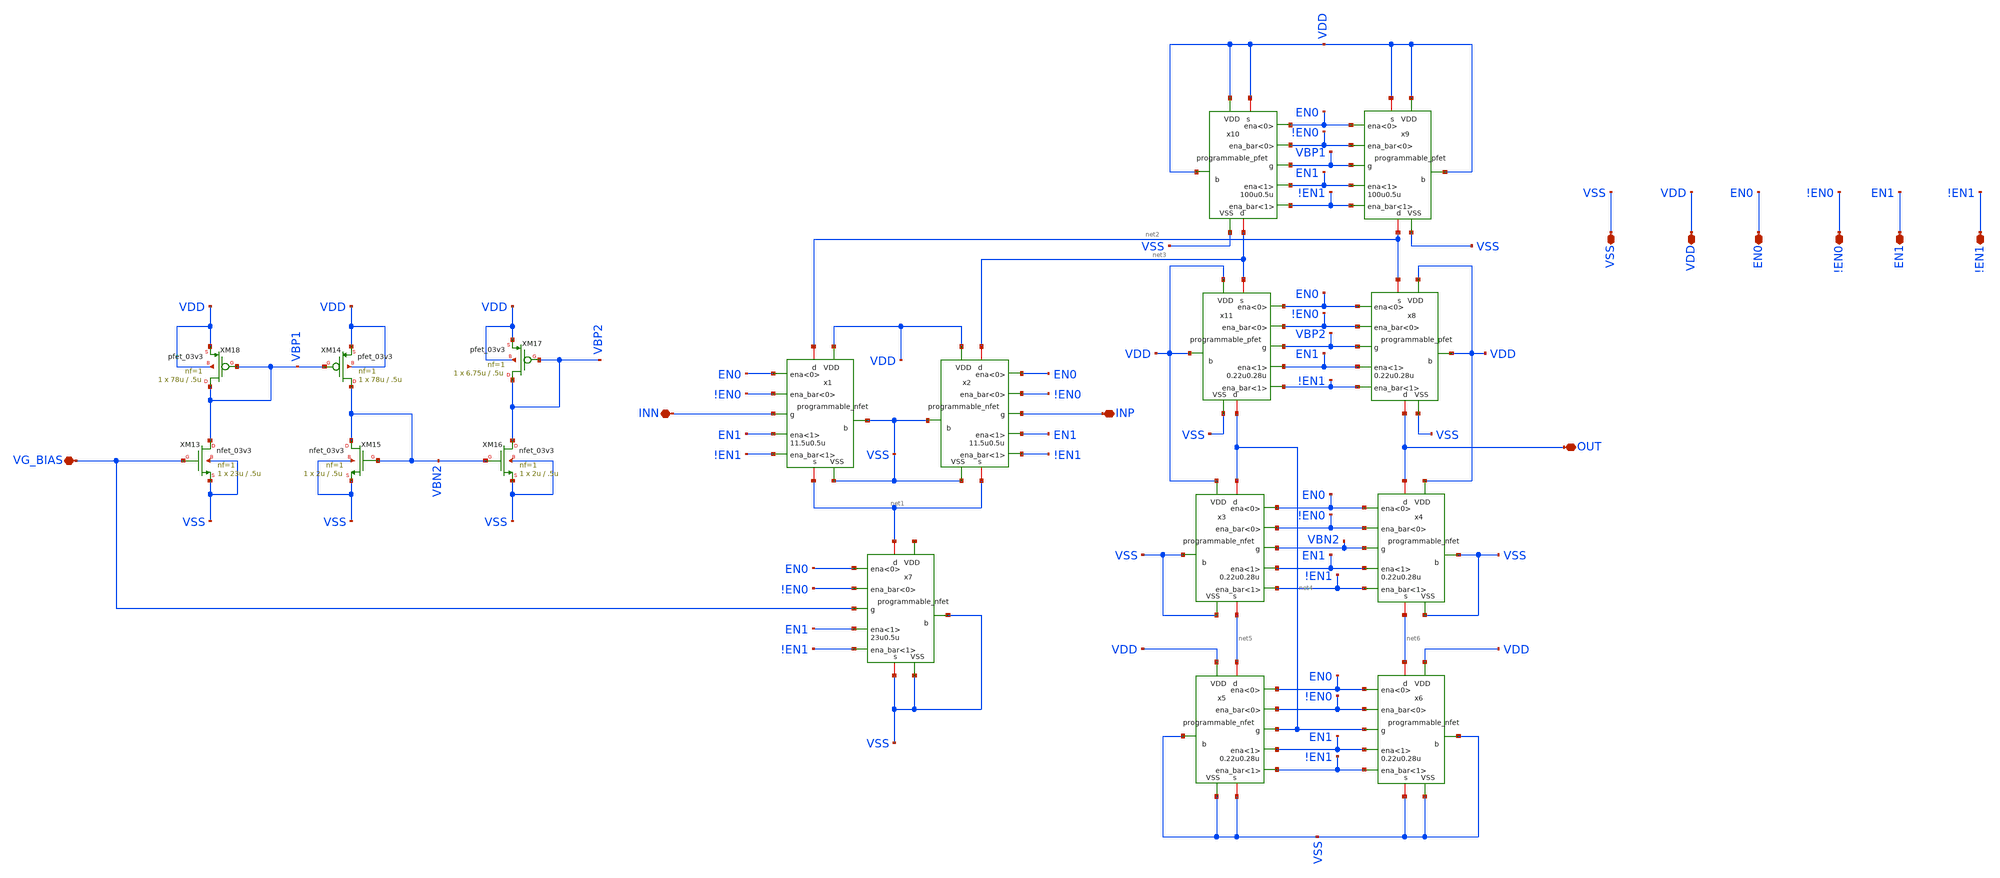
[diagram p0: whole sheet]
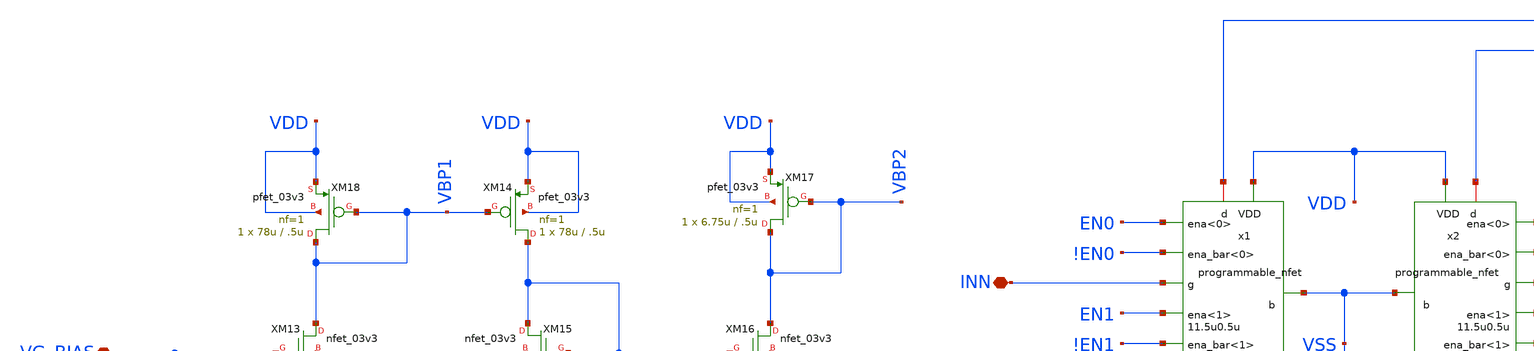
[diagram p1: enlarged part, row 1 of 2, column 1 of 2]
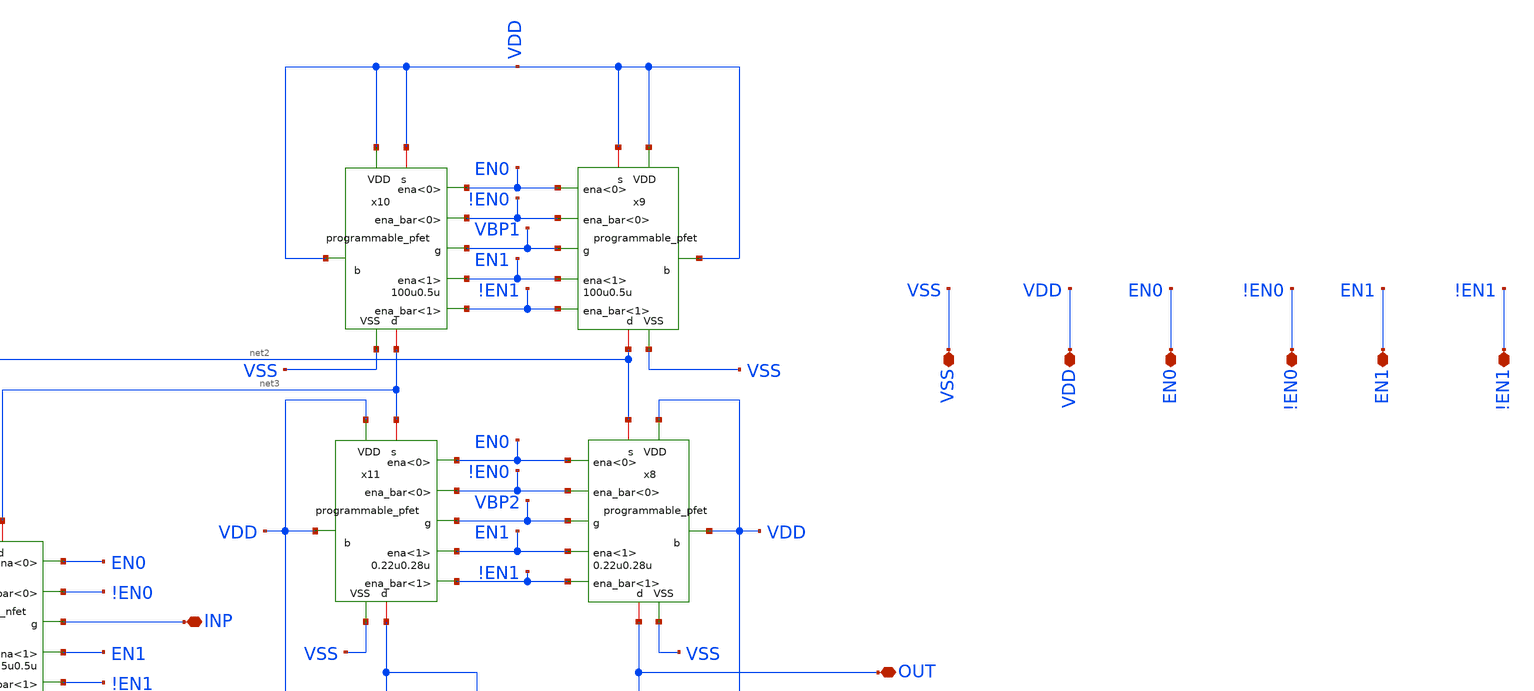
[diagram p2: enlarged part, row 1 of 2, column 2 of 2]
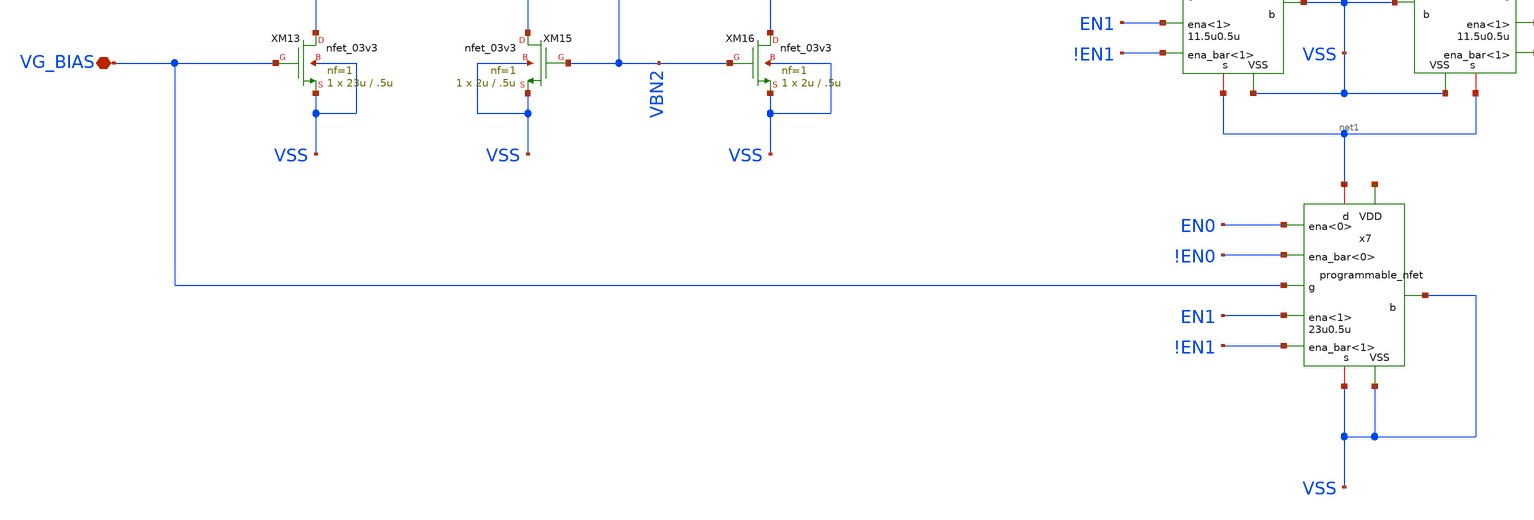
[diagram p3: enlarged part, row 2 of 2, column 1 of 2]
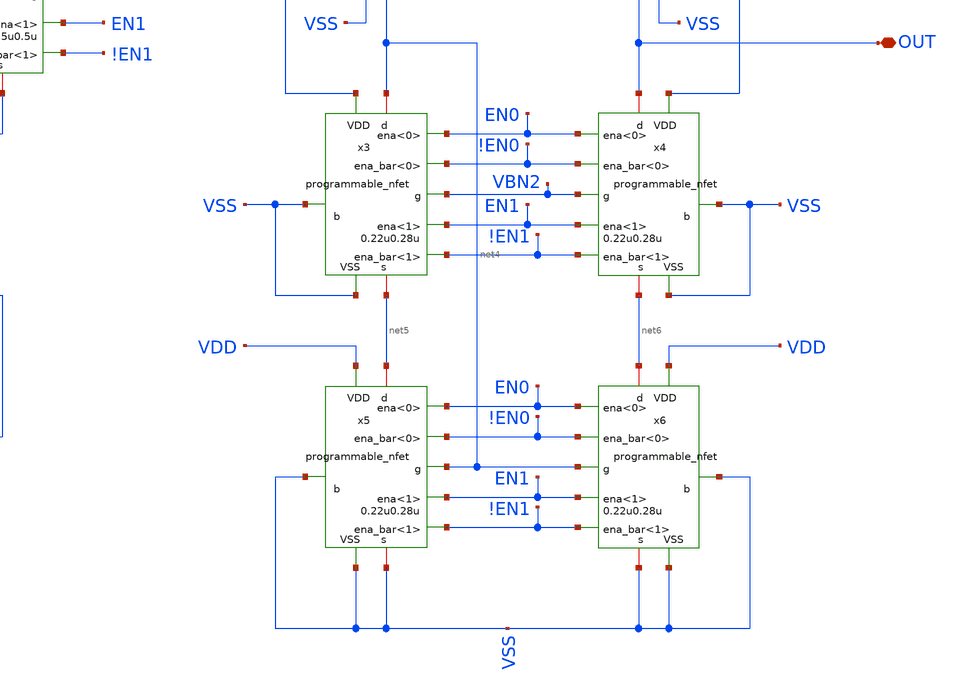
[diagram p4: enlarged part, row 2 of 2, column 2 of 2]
** sch_path: designs/libs/core_amps/ota_folded_cascode/programmable_folded.sch
**.subckt programmable_folded OUT VSS VDD EN0 !EN0 EN1 !EN1 INN INP VG_BIAS
*.iopin OUT
*.iopin VSS
*.iopin VDD
*.iopin EN0
*.iopin !EN0
*.iopin EN1
*.iopin !EN1
*.iopin INN
*.iopin INP
*.iopin VG_BIAS
x1 net2 VSS INN net1 !EN0 VDD !EN1 EN0 EN1 VSS programmable_nfet width=11.5u length=0.5u
x2 net3 VSS INP net1 !EN0 VDD !EN1 EN0 EN1 VSS programmable_nfet width=11.5u length=0.5u
x3 net4 VSS VBN2 net5 !EN0 VDD !EN1 EN0 EN1 VSS programmable_nfet width=0.22u length=0.28u
x4 OUT VSS VBN2 net6 !EN0 VDD !EN1 EN0 EN1 VSS programmable_nfet width=0.22u length=0.28u
x5 net5 VSS net4 VSS !EN0 VDD !EN1 EN0 EN1 VSS programmable_nfet width=0.22u length=0.28u
x6 net6 VSS net4 VSS !EN0 VDD !EN1 EN0 EN1 VSS programmable_nfet width=0.22u length=0.28u
x7 net1 VSS VG_BIAS VSS !EN0 net7 !EN1 EN0 EN1 VSS programmable_nfet width=23u length=0.5u
x8 OUT VDD VBP2 net2 !EN0 VDD !EN1 EN0 EN1 VSS programmable_pfet width=0.22u length=0.28u
x9 net2 VDD VBP1 VDD !EN0 VDD !EN1 EN0 EN1 VSS programmable_pfet width=100u length=0.5u
x10 net3 VDD VBP1 VDD !EN0 VDD !EN1 EN0 EN1 VSS programmable_pfet width=100u length=0.5u
x11 net4 VDD VBP2 net3 !EN0 VDD !EN1 EN0 EN1 VSS programmable_pfet width=0.22u length=0.28u
XM18 VBP1 VBP1 VDD VDD pfet_03v3 L=.5u W=78u nf=1 ad='int((nf+1)/2) * W/nf * 0.18u' as='int((nf+2)/2) * W/nf * 0.18u'
+ pd='2*int((nf+1)/2) * (W/nf + 0.18u)' ps='2*int((nf+2)/2) * (W/nf + 0.18u)' nrd='0.18u / W' nrs='0.18u / W'
+ sa=0 sb=0 sd=0 m=1
XM13 VBP1 VG_BIAS VSS VSS nfet_03v3 L=.5u W=23u nf=1 ad='int((nf+1)/2) * W/nf * 0.18u' as='int((nf+2)/2) * W/nf * 0.18u'
+ pd='2*int((nf+1)/2) * (W/nf + 0.18u)' ps='2*int((nf+2)/2) * (W/nf + 0.18u)' nrd='0.18u / W' nrs='0.18u / W'
+ sa=0 sb=0 sd=0 m=1
XM14 VBN2 VBP1 VDD VDD pfet_03v3 L=.5u W=78u nf=1 ad='int((nf+1)/2) * W/nf * 0.18u' as='int((nf+2)/2) * W/nf * 0.18u'
+ pd='2*int((nf+1)/2) * (W/nf + 0.18u)' ps='2*int((nf+2)/2) * (W/nf + 0.18u)' nrd='0.18u / W' nrs='0.18u / W'
+ sa=0 sb=0 sd=0 m=1
XM15 VBN2 VBN2 VSS VSS nfet_03v3 L=.5u W=2u nf=1 ad='int((nf+1)/2) * W/nf * 0.18u' as='int((nf+2)/2) * W/nf * 0.18u'
+ pd='2*int((nf+1)/2) * (W/nf + 0.18u)' ps='2*int((nf+2)/2) * (W/nf + 0.18u)' nrd='0.18u / W' nrs='0.18u / W'
+ sa=0 sb=0 sd=0 m=1
XM16 VBP2 VBN2 VSS VSS nfet_03v3 L=.5u W=2u nf=1 ad='int((nf+1)/2) * W/nf * 0.18u' as='int((nf+2)/2) * W/nf * 0.18u'
+ pd='2*int((nf+1)/2) * (W/nf + 0.18u)' ps='2*int((nf+2)/2) * (W/nf + 0.18u)' nrd='0.18u / W' nrs='0.18u / W'
+ sa=0 sb=0 sd=0 m=1
XM17 VBP2 VBP2 VDD VDD pfet_03v3 L=.5u W=6.75u nf=1 ad='int((nf+1)/2) * W/nf * 0.18u' as='int((nf+2)/2) * W/nf * 0.18u'
+ pd='2*int((nf+1)/2) * (W/nf + 0.18u)' ps='2*int((nf+2)/2) * (W/nf + 0.18u)' nrd='0.18u / W' nrs='0.18u / W'
+ sa=0 sb=0 sd=0 m=1
**.ends

* expanding   symbol:  libs/core_digital/programmable_nfet.sym # of pins=10
** sym_path: designs/libs/core_digital/programmable_nfet.sym
** sch_path: designs/libs/core_digital/programmable_nfet.sch
.subckt programmable_nfet d b g s ena_bar<0> VDD ena_bar<1> ena<0> ena<1> VSS  width=0.22u
+ length=0.28u
*.ipin VSS
*.ipin VDD
*.ipin g
*.ipin ena_bar<1>
*.ipin ena_bar<0>
*.ipin ena<1>
*.ipin ena<0>
*.iopin d
*.iopin s
*.ipin b
XM1 d net2 s b nfet_03v3 L={length} W={width} nf={nf} ad='int((nf+1)/2) * W/nf * 0.18u' as='int((nf+2)/2) * W/nf * 0.18u'
+ pd='2*int((nf+1)/2) * (W/nf + 0.18u)' ps='2*int((nf+2)/2) * (W/nf + 0.18u)' nrd='0.18u / W' nrs='0.18u / W'
+ sa=0 sb=0 sd=0 m={mult}
XM3 d net1 s b nfet_03v3 L={length} W={2*width} nf={2*nf} ad='int((nf+1)/2) * W/nf * 0.18u' as='int((nf+2)/2) * W/nf * 0.18u'
+ pd='2*int((nf+1)/2) * (W/nf + 0.18u)' ps='2*int((nf+2)/2) * (W/nf + 0.18u)' nrd='0.18u / W' nrs='0.18u / W'
+ sa=0 sb=0 sd=0 m={mult}
x1 ena_bar<0> VDD net2 g VSS ena<0> transmission_gate
x3 ena_bar<1> VDD net1 g VSS ena<1> transmission_gate
XM2 net1 ena_bar<1> VSS VSS nfet_03v3 L=0.28u W=0.22u nf=1 ad='int((nf+1)/2) * W/nf * 0.18u' as='int((nf+2)/2) * W/nf * 0.18u'
+ pd='2*int((nf+1)/2) * (W/nf + 0.18u)' ps='2*int((nf+2)/2) * (W/nf + 0.18u)' nrd='0.18u / W' nrs='0.18u / W'
+ sa=0 sb=0 sd=0 m=1
XM4 net2 ena_bar<0> VSS VSS nfet_03v3 L=0.28u W=0.22u nf=1 ad='int((nf+1)/2) * W/nf * 0.18u' as='int((nf+2)/2) * W/nf * 0.18u'
+ pd='2*int((nf+1)/2) * (W/nf + 0.18u)' ps='2*int((nf+2)/2) * (W/nf + 0.18u)' nrd='0.18u / W' nrs='0.18u / W'
+ sa=0 sb=0 sd=0 m=1
.ends


* expanding   symbol:  libs/core_digital/programmable_pfet.sym # of pins=10
** sym_path: designs/libs/core_digital/programmable_pfet.sym
** sch_path: designs/libs/core_digital/programmable_pfet.sch
.subckt programmable_pfet d b g s ena_bar<0> VDD ena_bar<1> ena<0> ena<1> VSS  width=0.22u
+ length=0.28u
*.ipin VSS
*.ipin VDD
*.ipin g
*.ipin ena_bar<1>
*.ipin ena_bar<0>
*.ipin ena<0>
*.iopin s
*.iopin d
*.ipin b
*.ipin ena<1>
x1 ena_bar<0> VDD net2 g VSS ena<0> transmission_gate
x3 ena_bar<1> VDD net1 g VSS ena<1> transmission_gate
XM1 d net2 s b pfet_03v3 L={length} W={width} nf=1 ad='int((nf+1)/2) * W/nf * 0.18u' as='int((nf+2)/2) * W/nf * 0.18u'
+ pd='2*int((nf+1)/2) * (W/nf + 0.18u)' ps='2*int((nf+2)/2) * (W/nf + 0.18u)' nrd='0.18u / W' nrs='0.18u / W'
+ sa=0 sb=0 sd=0 m=1
XM3 d net1 s b pfet_03v3 L={length} W={2*width} nf=1 ad='int((nf+1)/2) * W/nf * 0.18u' as='int((nf+2)/2) * W/nf * 0.18u'
+ pd='2*int((nf+1)/2) * (W/nf + 0.18u)' ps='2*int((nf+2)/2) * (W/nf + 0.18u)' nrd='0.18u / W' nrs='0.18u / W'
+ sa=0 sb=0 sd=0 m=1
XM2 net1 ena<1> VDD VDD pfet_03v3 L=0.28u W=0.22u nf=1 ad='int((nf+1)/2) * W/nf * 0.18u' as='int((nf+2)/2) * W/nf * 0.18u'
+ pd='2*int((nf+1)/2) * (W/nf + 0.18u)' ps='2*int((nf+2)/2) * (W/nf + 0.18u)' nrd='0.18u / W' nrs='0.18u / W'
+ sa=0 sb=0 sd=0 m=1
XM4 net2 ena<0> VDD VDD pfet_03v3 L=0.28u W=0.22u nf=1 ad='int((nf+1)/2) * W/nf * 0.18u' as='int((nf+2)/2) * W/nf * 0.18u'
+ pd='2*int((nf+1)/2) * (W/nf + 0.18u)' ps='2*int((nf+2)/2) * (W/nf + 0.18u)' nrd='0.18u / W' nrs='0.18u / W'
+ sa=0 sb=0 sd=0 m=1
.ends


* expanding   symbol:  libs/core_digital/transmission_gate.sym # of pins=6
** sym_path: designs/libs/core_digital/schem/transmission_gate.sym
** sch_path: designs/libs/core_digital/schem/transmission_gate.sch
.subckt transmission_gate ena_bar VDD out in VSS ena
*.ipin in
*.ipin ena_bar
*.ipin ena
*.ipin VSS
*.ipin VDD
*.opin out
XM1 in ena_bar out VDD pfet_03v3 L=0.28u W=0.22u nf=1 ad='int((nf+1)/2) * W/nf * 0.18u' as='int((nf+2)/2) * W/nf * 0.18u'
+ pd='2*int((nf+1)/2) * (W/nf + 0.18u)' ps='2*int((nf+2)/2) * (W/nf + 0.18u)' nrd='0.18u / W' nrs='0.18u / W'
+ sa=0 sb=0 sd=0 m=1
XM2 in ena out VSS nfet_03v3 L=0.28u W=0.22u nf=1 ad='int((nf+1)/2) * W/nf * 0.18u' as='int((nf+2)/2) * W/nf * 0.18u'
+ pd='2*int((nf+1)/2) * (W/nf + 0.18u)' ps='2*int((nf+2)/2) * (W/nf + 0.18u)' nrd='0.18u / W' nrs='0.18u / W'
+ sa=0 sb=0 sd=0 m=1
.ends

.end
